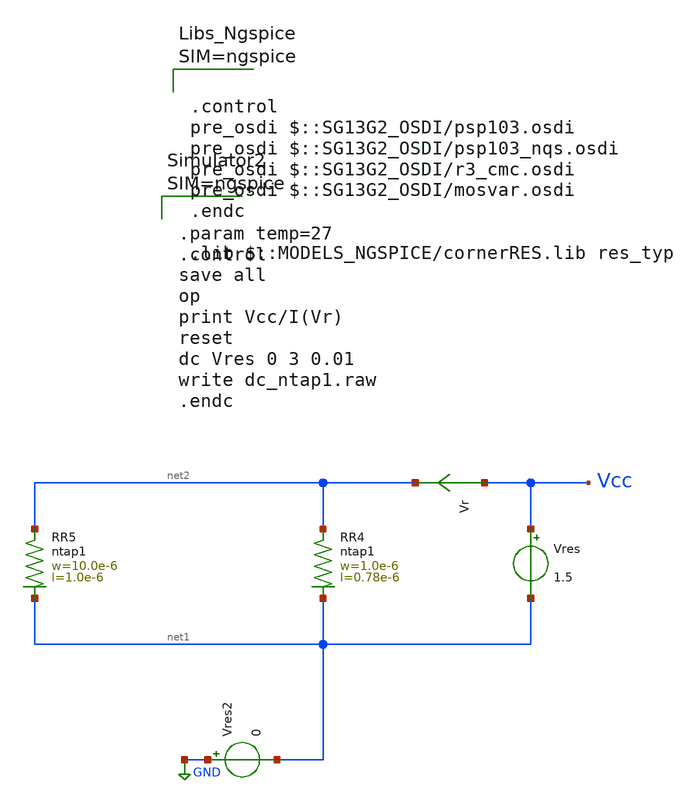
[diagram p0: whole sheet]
** sch_path: ihp-sg13g2/xschem_libs/sg13g2_tests/dc_ntap1/schematic/dc_ntap1.sch
* Copyright 2023 IHP PDK Authors
**.subckt dc_ntap1
Vres Vcc net1 1.5
Vr Vcc net2 0
.save i(vr)
Vres2 GND net1 0
XR4 net2 net1 ntap1 R=225.8 w=1.0e-6 l=0.78e-6
XR5 net2 net1 ntap1 R=30.62 w=10.0e-6 l=1.0e-6
**** begin user architecture code

.control
pre_osdi $::SG13G2_OSDI/psp103.osdi
pre_osdi $::SG13G2_OSDI/psp103_nqs.osdi
pre_osdi $::SG13G2_OSDI/r3_cmc.osdi
pre_osdi $::SG13G2_OSDI/mosvar.osdi
.endc

.lib $::MODELS_NGSPICE/cornerRES.lib res_typ




.param temp=27
.control
save all
op
print Vcc/I(Vr)
reset
dc Vres 0 3 0.01
write dc_ntap1.raw
.endc



**** end user architecture code
**.ends
.GLOBAL GND
.end
